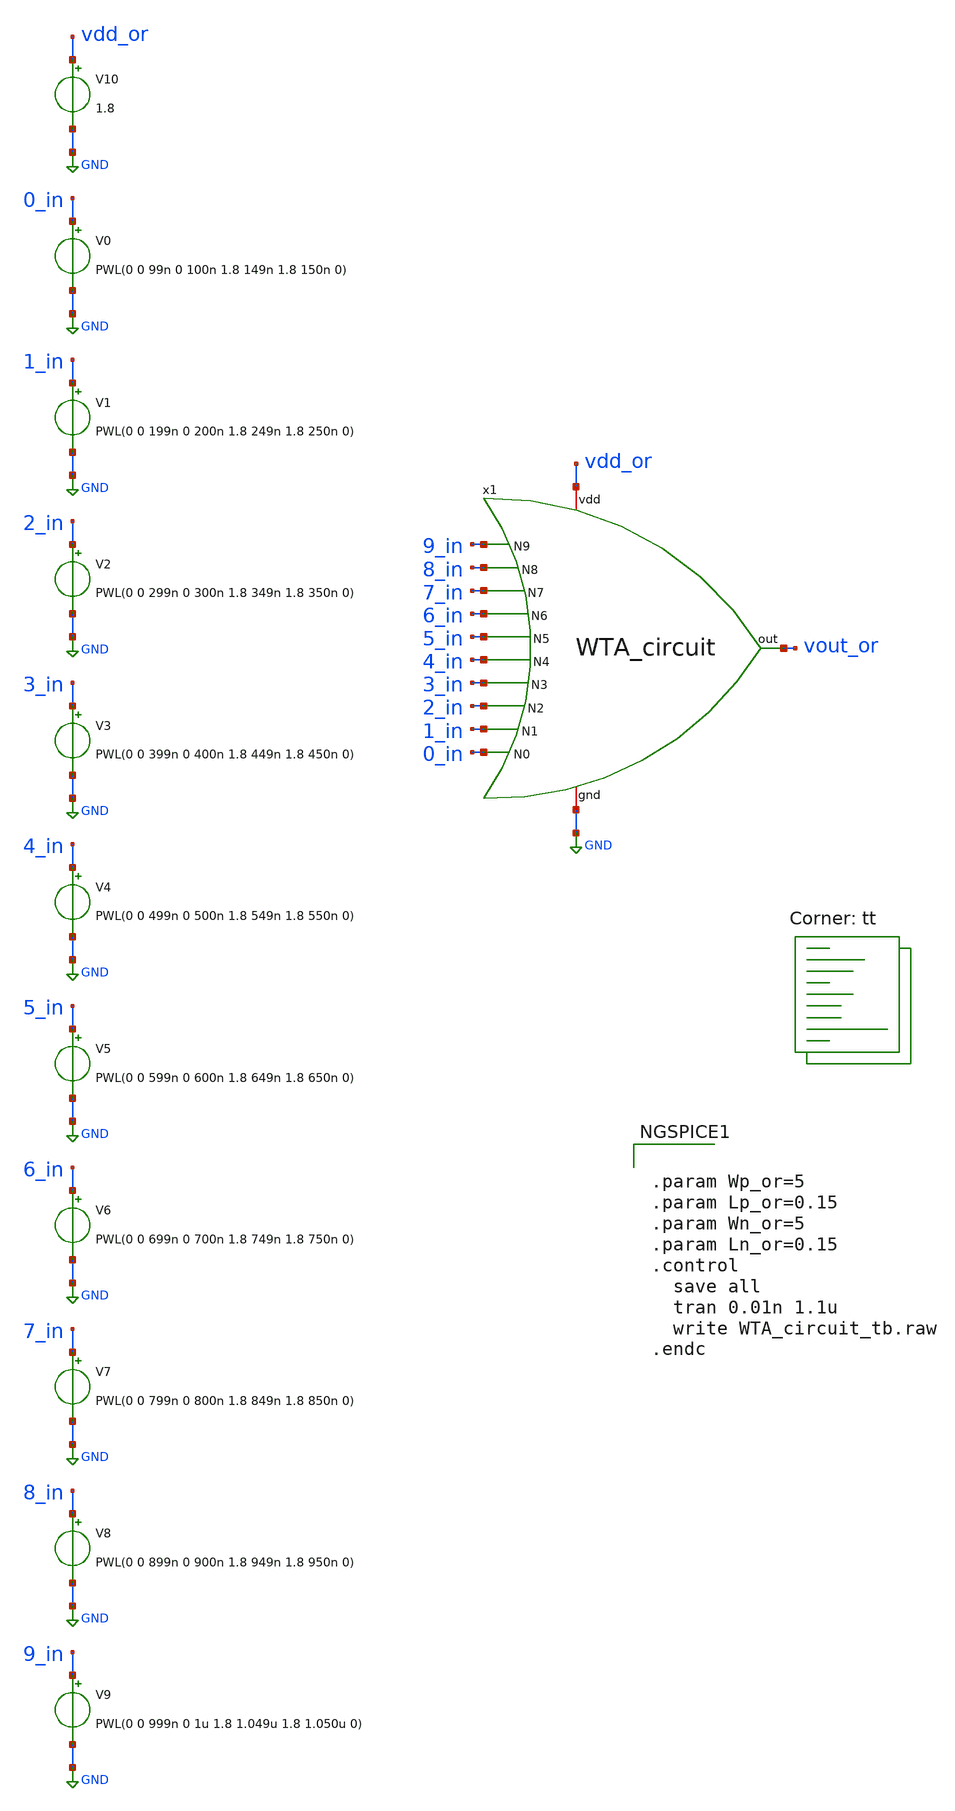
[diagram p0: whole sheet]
** sch_path: inhibitory/WTA_circuit_tb.sch
**.subckt WTA_circuit_tb
V0 0_in GND PWL(0 0 99n 0 100n 1.8 149n 1.8 150n 0)
V10 vdd_or GND 1.8
x1 vdd_or 9_in 8_in 7_in 6_in 5_in 4_in 3_in 2_in 1_in 0_in vout_or GND WTA_circuit
V1 1_in GND PWL(0 0 199n 0 200n 1.8 249n 1.8 250n 0)
V2 2_in GND PWL(0 0 299n 0 300n 1.8 349n 1.8 350n 0)
V3 3_in GND PWL(0 0 399n 0 400n 1.8 449n 1.8 450n 0)
V4 4_in GND PWL(0 0 499n 0 500n 1.8 549n 1.8 550n 0)
V5 5_in GND PWL(0 0 599n 0 600n 1.8 649n 1.8 650n 0)
V6 6_in GND PWL(0 0 699n 0 700n 1.8 749n 1.8 750n 0)
V7 7_in GND PWL(0 0 799n 0 800n 1.8 849n 1.8 850n 0)
V8 8_in GND PWL(0 0 899n 0 900n 1.8 949n 1.8 950n 0)
V9 9_in GND PWL(0 0 999n 0 1u 1.8 1.049u 1.8 1.050u 0)
**** begin user architecture code
.lib $::SKYWATER_MODELS/sky130.lib.spice tt


.param Wp_or=5
.param Lp_or=0.15
.param Wn_or=5
.param Ln_or=0.15
.control
  save all
  tran 0.01n 1.1u
  write WTA_circuit_tb.raw
.endc

**** end user architecture code
**.ends

* expanding   symbol:  /home/ricardo/RATT_repos/Proyectos_xschem/inhibitory/WTA_circuit.sym # of
*+ pins=13
** sym_path: inhibitory/WTA_circuit.sym
** sch_path: inhibitory/WTA_circuit.sch
.subckt WTA_circuit vdd N9 N8 N7 N6 N5 N4 N3 N2 N1 N0 out gnd
*.iopin gnd
*.ipin N0
*.ipin N1
*.opin out
*.iopin vdd
*.ipin N2
*.ipin N3
*.ipin N4
*.ipin N5
*.ipin N6
*.ipin N7
*.ipin N8
*.ipin N9
XM5 net1 N1 net2 vdd sky130_fd_pr__pfet_01v8 L={Lp_or} W={Wp_or} nf=1 ad='int((nf+1)/2) * W/nf * 0.29'
+ as='int((nf+2)/2) * W/nf * 0.29' pd='2*int((nf+1)/2) * (W/nf + 0.29)' ps='2*int((nf+2)/2) * (W/nf + 0.29)'
+ nrd='0.29 / W' nrs='0.29 / W' sa=0 sb=0 sd=0 mult=1 m=1
XM6 net3 N1 gnd gnd sky130_fd_pr__nfet_01v8 L={Ln_or} W={Wn_or} nf=1 ad='int((nf+1)/2) * W/nf * 0.29'
+ as='int((nf+2)/2) * W/nf * 0.29' pd='2*int((nf+1)/2) * (W/nf + 0.29)' ps='2*int((nf+2)/2) * (W/nf + 0.29)'
+ nrd='0.29 / W' nrs='0.29 / W' sa=0 sb=0 sd=0 mult=1 m=1
XM3 net3 N0 net1 vdd sky130_fd_pr__pfet_01v8 L={Lp_or} W={Wp_or} nf=1 ad='int((nf+1)/2) * W/nf * 0.29'
+ as='int((nf+2)/2) * W/nf * 0.29' pd='2*int((nf+1)/2) * (W/nf + 0.29)' ps='2*int((nf+2)/2) * (W/nf + 0.29)'
+ nrd='0.29 / W' nrs='0.29 / W' sa=0 sb=0 sd=0 mult=1 m=1
XM4 net3 N0 gnd gnd sky130_fd_pr__nfet_01v8 L={Ln_or} W={Wn_or} nf=1 ad='int((nf+1)/2) * W/nf * 0.29'
+ as='int((nf+2)/2) * W/nf * 0.29' pd='2*int((nf+1)/2) * (W/nf + 0.29)' ps='2*int((nf+2)/2) * (W/nf + 0.29)'
+ nrd='0.29 / W' nrs='0.29 / W' sa=0 sb=0 sd=0 mult=1 m=1
XM2 out net3 gnd gnd sky130_fd_pr__nfet_01v8 L={Ln_or} W={Wn_or} nf=1 ad='int((nf+1)/2) * W/nf * 0.29'
+ as='int((nf+2)/2) * W/nf * 0.29' pd='2*int((nf+1)/2) * (W/nf + 0.29)' ps='2*int((nf+2)/2) * (W/nf + 0.29)'
+ nrd='0.29 / W' nrs='0.29 / W' sa=0 sb=0 sd=0 mult=1 m=1
XM1 out net3 vdd vdd sky130_fd_pr__pfet_01v8 L={Lp_or} W={Wp_or} nf=1 ad='int((nf+1)/2) * W/nf * 0.29'
+ as='int((nf+2)/2) * W/nf * 0.29' pd='2*int((nf+1)/2) * (W/nf + 0.29)' ps='2*int((nf+2)/2) * (W/nf + 0.29)'
+ nrd='0.29 / W' nrs='0.29 / W' sa=0 sb=0 sd=0 mult=1 m=1
XM7 net2 N2 net4 vdd sky130_fd_pr__pfet_01v8 L={Lp_or} W={Wp_or} nf=1 ad='int((nf+1)/2) * W/nf * 0.29'
+ as='int((nf+2)/2) * W/nf * 0.29' pd='2*int((nf+1)/2) * (W/nf + 0.29)' ps='2*int((nf+2)/2) * (W/nf + 0.29)'
+ nrd='0.29 / W' nrs='0.29 / W' sa=0 sb=0 sd=0 mult=1 m=1
XM8 net3 N2 gnd gnd sky130_fd_pr__nfet_01v8 L={Ln_or} W={Wn_or} nf=1 ad='int((nf+1)/2) * W/nf * 0.29'
+ as='int((nf+2)/2) * W/nf * 0.29' pd='2*int((nf+1)/2) * (W/nf + 0.29)' ps='2*int((nf+2)/2) * (W/nf + 0.29)'
+ nrd='0.29 / W' nrs='0.29 / W' sa=0 sb=0 sd=0 mult=1 m=1
XM9 net4 N3 net5 vdd sky130_fd_pr__pfet_01v8 L={Lp_or} W={Wp_or} nf=1 ad='int((nf+1)/2) * W/nf * 0.29'
+ as='int((nf+2)/2) * W/nf * 0.29' pd='2*int((nf+1)/2) * (W/nf + 0.29)' ps='2*int((nf+2)/2) * (W/nf + 0.29)'
+ nrd='0.29 / W' nrs='0.29 / W' sa=0 sb=0 sd=0 mult=1 m=1
XM11 net5 N4 net6 vdd sky130_fd_pr__pfet_01v8 L={Lp_or} W={Wp_or} nf=1 ad='int((nf+1)/2) * W/nf * 0.29'
+ as='int((nf+2)/2) * W/nf * 0.29' pd='2*int((nf+1)/2) * (W/nf + 0.29)' ps='2*int((nf+2)/2) * (W/nf + 0.29)'
+ nrd='0.29 / W' nrs='0.29 / W' sa=0 sb=0 sd=0 mult=1 m=1
XM13 net6 N5 net7 vdd sky130_fd_pr__pfet_01v8 L={Lp_or} W={Wp_or} nf=1 ad='int((nf+1)/2) * W/nf * 0.29'
+ as='int((nf+2)/2) * W/nf * 0.29' pd='2*int((nf+1)/2) * (W/nf + 0.29)' ps='2*int((nf+2)/2) * (W/nf + 0.29)'
+ nrd='0.29 / W' nrs='0.29 / W' sa=0 sb=0 sd=0 mult=1 m=1
XM15 net7 N6 net8 vdd sky130_fd_pr__pfet_01v8 L={Lp_or} W={Wp_or} nf=1 ad='int((nf+1)/2) * W/nf * 0.29'
+ as='int((nf+2)/2) * W/nf * 0.29' pd='2*int((nf+1)/2) * (W/nf + 0.29)' ps='2*int((nf+2)/2) * (W/nf + 0.29)'
+ nrd='0.29 / W' nrs='0.29 / W' sa=0 sb=0 sd=0 mult=1 m=1
XM17 net8 N7 net9 vdd sky130_fd_pr__pfet_01v8 L={Lp_or} W={Wp_or} nf=1 ad='int((nf+1)/2) * W/nf * 0.29'
+ as='int((nf+2)/2) * W/nf * 0.29' pd='2*int((nf+1)/2) * (W/nf + 0.29)' ps='2*int((nf+2)/2) * (W/nf + 0.29)'
+ nrd='0.29 / W' nrs='0.29 / W' sa=0 sb=0 sd=0 mult=1 m=1
XM19 net9 N8 net10 vdd sky130_fd_pr__pfet_01v8 L={Lp_or} W={Wp_or} nf=1 ad='int((nf+1)/2) * W/nf * 0.29'
+ as='int((nf+2)/2) * W/nf * 0.29' pd='2*int((nf+1)/2) * (W/nf + 0.29)' ps='2*int((nf+2)/2) * (W/nf + 0.29)'
+ nrd='0.29 / W' nrs='0.29 / W' sa=0 sb=0 sd=0 mult=1 m=1
XM21 net10 N9 vdd vdd sky130_fd_pr__pfet_01v8 L={Lp_or} W={Wp_or} nf=1 ad='int((nf+1)/2) * W/nf * 0.29'
+ as='int((nf+2)/2) * W/nf * 0.29' pd='2*int((nf+1)/2) * (W/nf + 0.29)' ps='2*int((nf+2)/2) * (W/nf + 0.29)'
+ nrd='0.29 / W' nrs='0.29 / W' sa=0 sb=0 sd=0 mult=1 m=1
XM10 net3 N3 gnd gnd sky130_fd_pr__nfet_01v8 L={Ln_or} W={Wn_or} nf=1 ad='int((nf+1)/2) * W/nf * 0.29'
+ as='int((nf+2)/2) * W/nf * 0.29' pd='2*int((nf+1)/2) * (W/nf + 0.29)' ps='2*int((nf+2)/2) * (W/nf + 0.29)'
+ nrd='0.29 / W' nrs='0.29 / W' sa=0 sb=0 sd=0 mult=1 m=1
XM12 net3 N4 gnd gnd sky130_fd_pr__nfet_01v8 L={Ln_or} W={Wn_or} nf=1 ad='int((nf+1)/2) * W/nf * 0.29'
+ as='int((nf+2)/2) * W/nf * 0.29' pd='2*int((nf+1)/2) * (W/nf + 0.29)' ps='2*int((nf+2)/2) * (W/nf + 0.29)'
+ nrd='0.29 / W' nrs='0.29 / W' sa=0 sb=0 sd=0 mult=1 m=1
XM14 net3 N5 gnd gnd sky130_fd_pr__nfet_01v8 L={Ln_or} W={Wn_or} nf=1 ad='int((nf+1)/2) * W/nf * 0.29'
+ as='int((nf+2)/2) * W/nf * 0.29' pd='2*int((nf+1)/2) * (W/nf + 0.29)' ps='2*int((nf+2)/2) * (W/nf + 0.29)'
+ nrd='0.29 / W' nrs='0.29 / W' sa=0 sb=0 sd=0 mult=1 m=1
XM16 net3 N6 gnd gnd sky130_fd_pr__nfet_01v8 L={Ln_or} W={Wn_or} nf=1 ad='int((nf+1)/2) * W/nf * 0.29'
+ as='int((nf+2)/2) * W/nf * 0.29' pd='2*int((nf+1)/2) * (W/nf + 0.29)' ps='2*int((nf+2)/2) * (W/nf + 0.29)'
+ nrd='0.29 / W' nrs='0.29 / W' sa=0 sb=0 sd=0 mult=1 m=1
XM18 net3 N7 gnd gnd sky130_fd_pr__nfet_01v8 L={Ln_or} W={Wn_or} nf=1 ad='int((nf+1)/2) * W/nf * 0.29'
+ as='int((nf+2)/2) * W/nf * 0.29' pd='2*int((nf+1)/2) * (W/nf + 0.29)' ps='2*int((nf+2)/2) * (W/nf + 0.29)'
+ nrd='0.29 / W' nrs='0.29 / W' sa=0 sb=0 sd=0 mult=1 m=1
XM20 net3 N8 gnd gnd sky130_fd_pr__nfet_01v8 L={Ln_or} W={Wn_or} nf=1 ad='int((nf+1)/2) * W/nf * 0.29'
+ as='int((nf+2)/2) * W/nf * 0.29' pd='2*int((nf+1)/2) * (W/nf + 0.29)' ps='2*int((nf+2)/2) * (W/nf + 0.29)'
+ nrd='0.29 / W' nrs='0.29 / W' sa=0 sb=0 sd=0 mult=1 m=1
XM22 net3 N9 gnd gnd sky130_fd_pr__nfet_01v8 L={Ln_or} W={Wn_or} nf=1 ad='int((nf+1)/2) * W/nf * 0.29'
+ as='int((nf+2)/2) * W/nf * 0.29' pd='2*int((nf+1)/2) * (W/nf + 0.29)' ps='2*int((nf+2)/2) * (W/nf + 0.29)'
+ nrd='0.29 / W' nrs='0.29 / W' sa=0 sb=0 sd=0 mult=1 m=1
.ends

.GLOBAL GND
.end
